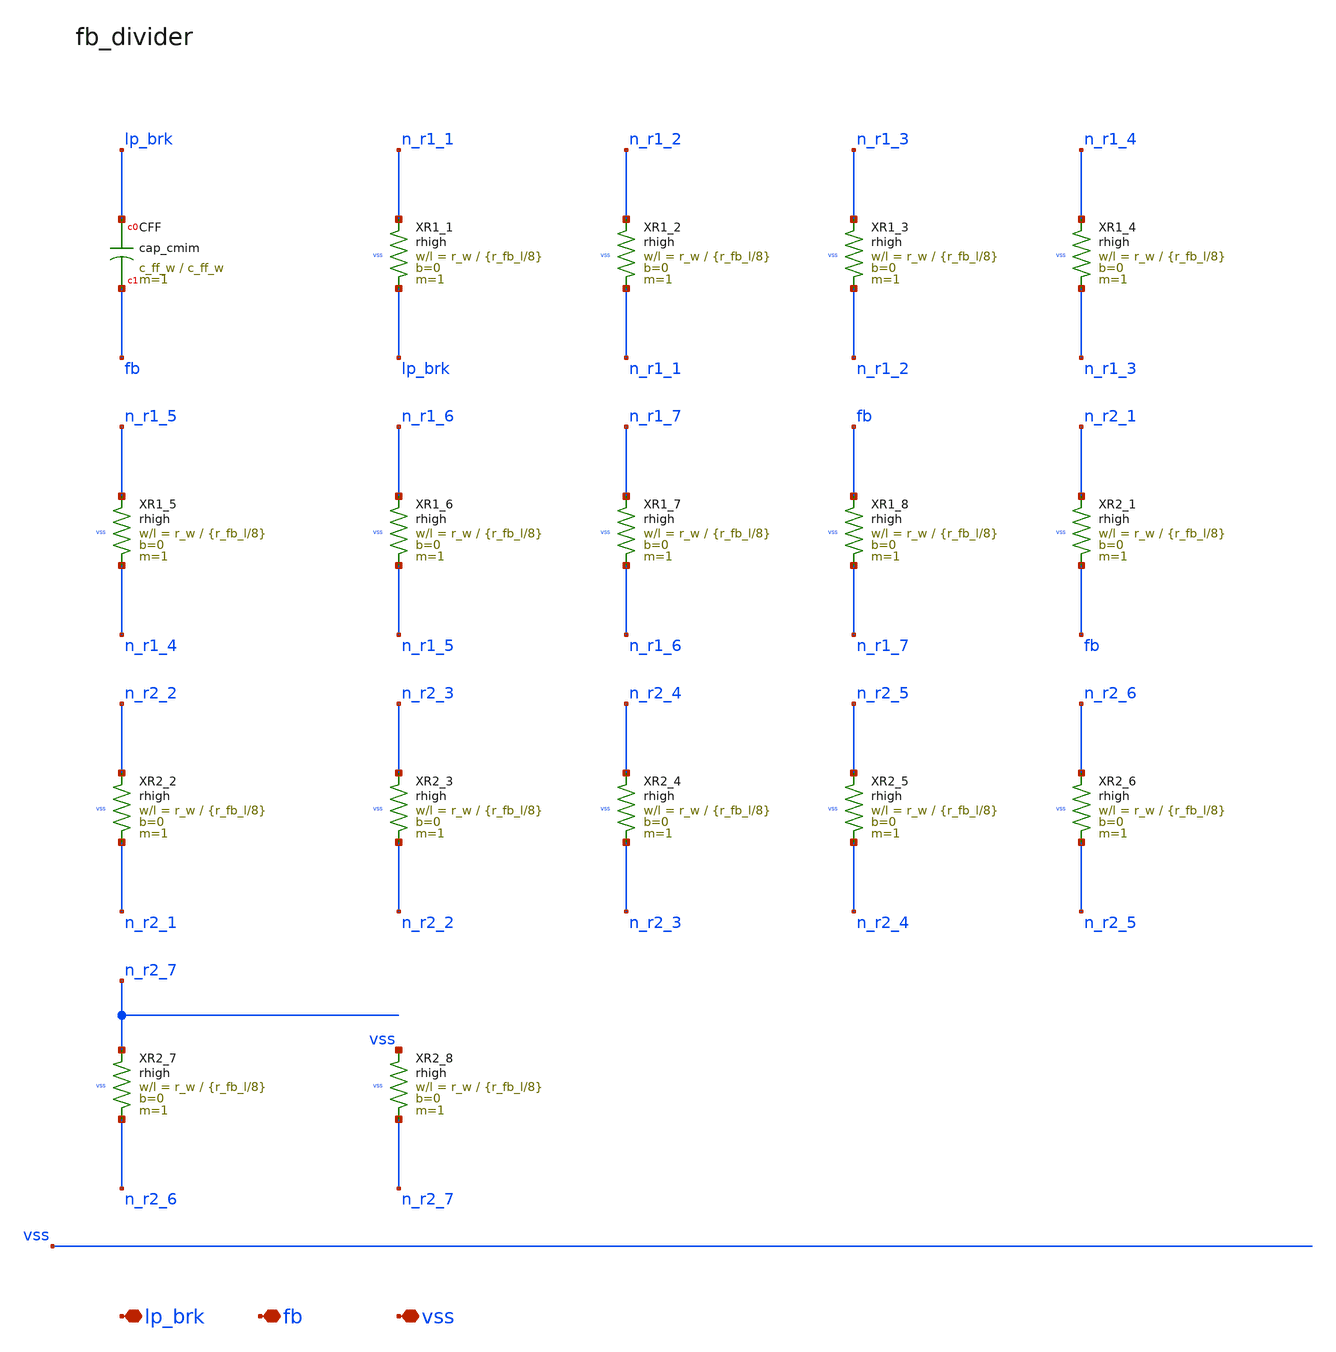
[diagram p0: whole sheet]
** sch_path: analog-db/circuits/ldo_010_capless_lowiq/pdk/ihp-sg13g2/schematic/blocks/fb_divider.sch
**.subckt fb_divider lp_brk fb vss
*.iopin lp_brk
*.iopin fb
*.iopin vss
XR1_1 lp_brk n_r1_1 vss rhigh w=r_w l={r_fb_l/8} m=1 b=0
XR1_2 n_r1_1 n_r1_2 vss rhigh w=r_w l={r_fb_l/8} m=1 b=0
XR1_3 n_r1_2 n_r1_3 vss rhigh w=r_w l={r_fb_l/8} m=1 b=0
XR1_4 n_r1_3 n_r1_4 vss rhigh w=r_w l={r_fb_l/8} m=1 b=0
XR1_5 n_r1_4 n_r1_5 vss rhigh w=r_w l={r_fb_l/8} m=1 b=0
XR1_6 n_r1_5 n_r1_6 vss rhigh w=r_w l={r_fb_l/8} m=1 b=0
XR1_7 n_r1_6 n_r1_7 vss rhigh w=r_w l={r_fb_l/8} m=1 b=0
XR1_8 n_r1_7 fb vss rhigh w=r_w l={r_fb_l/8} m=1 b=0
XR2_1 fb n_r2_1 vss rhigh w=r_w l={r_fb_l/8} m=1 b=0
XR2_2 n_r2_1 n_r2_2 vss rhigh w=r_w l={r_fb_l/8} m=1 b=0
XR2_3 n_r2_2 n_r2_3 vss rhigh w=r_w l={r_fb_l/8} m=1 b=0
XR2_4 n_r2_3 n_r2_4 vss rhigh w=r_w l={r_fb_l/8} m=1 b=0
XR2_5 n_r2_4 n_r2_5 vss rhigh w=r_w l={r_fb_l/8} m=1 b=0
XR2_6 n_r2_5 n_r2_6 vss rhigh w=r_w l={r_fb_l/8} m=1 b=0
XR2_7 n_r2_6 n_r2_7 vss rhigh w=r_w l={r_fb_l/8} m=1 b=0
XR2_8 n_r2_7 vss vss rhigh w=r_w l={r_fb_l/8} m=1 b=0
XCFF lp_brk fb cap_cmim w=c_ff_w l=c_ff_w m=1
**.ends
.end
